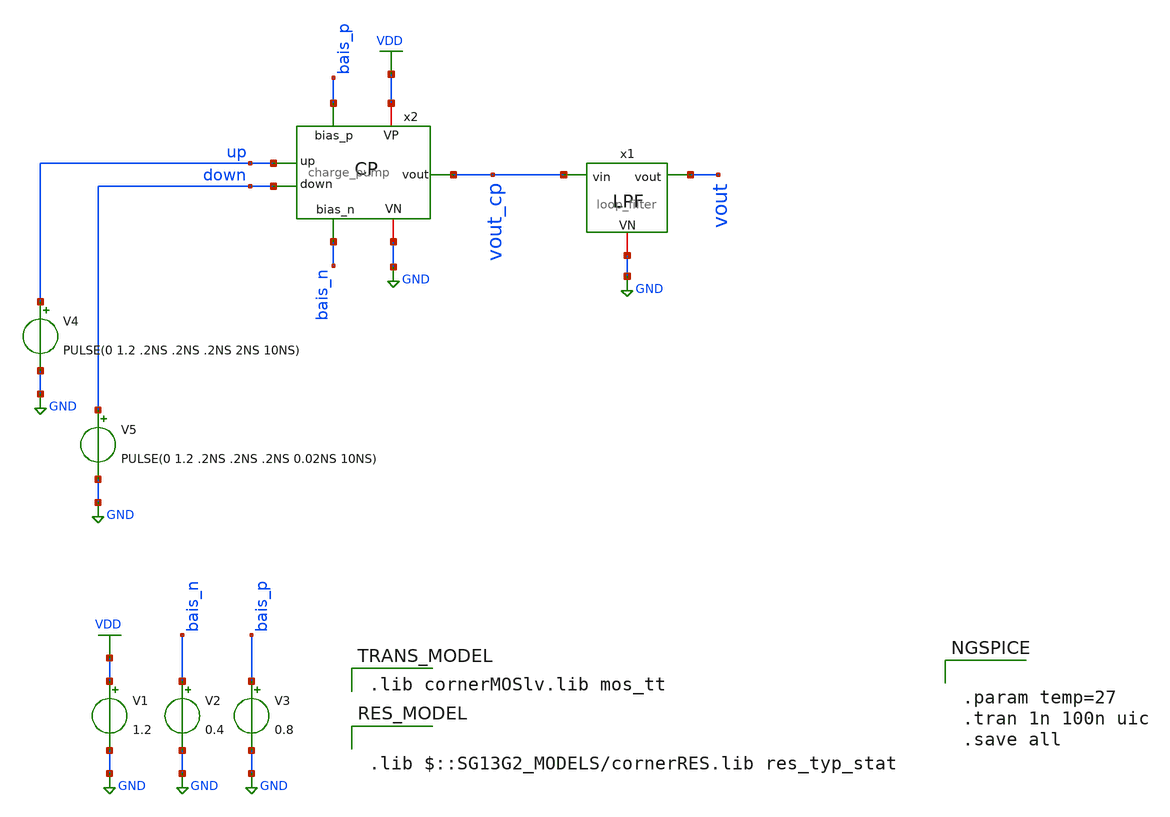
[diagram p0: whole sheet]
** sch_path: Combined Design/design_data/xschem/charge_pump_tb.sch
**.subckt charge_pump_tb
V1 VDD GND 1.2
V2 bais_n GND 0.4
V3 bais_p GND 0.8
V4 up GND PULSE(0 1.2 .2NS .2NS .2NS 2NS 10NS)
V5 down GND PULSE(0 1.2 .2NS .2NS .2NS 0.02NS 10NS)
x2 VDD bais_p up vout_cp down bais_n GND charge_pump
x1 vout_cp vout GND loop_filter
**** begin user architecture code


.param temp=27
.tran 1n 100n uic
.save all


 .lib cornerMOSlv.lib mos_tt


.lib $::SG13G2_MODELS/cornerRES.lib res_typ_stat

**** end user architecture code
**.ends
.GLOBAL GND
.GLOBAL VDD
.end
